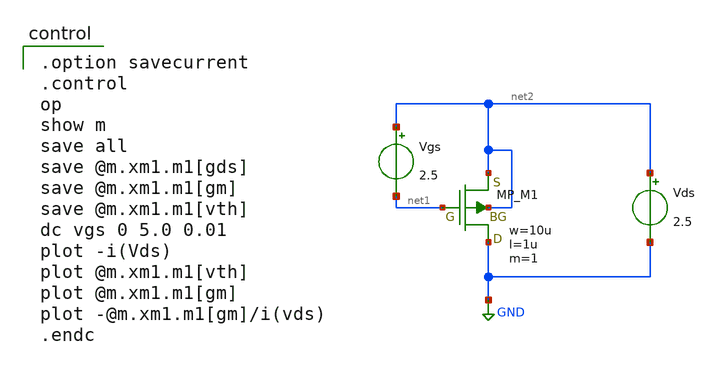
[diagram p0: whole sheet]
** sch_path: OpenSUSI-TR10/opamp/pfet_idvgs.sch
**.subckt pfet_idvgs
Vgs net2 net1 2.5
Vds net2 GND 2.5
XM1 GND net1 net2 net2 PMOS w=10u l=1u as=0 ad=0 ps=0 pd=0 nrd=0 nrs=0 m=1
**** begin user architecture code

.option savecurrent
.control
op
show m
save all
save @m.xm1.m1[gds]
save @m.xm1.m1[gm]
save @m.xm1.m1[vth]
dc vgs 0 5.0 0.01
plot -i(Vds)
plot @m.xm1.m1[vth]
plot @m.xm1.m1[gm]
plot -@m.xm1.m1[gm]/i(vds)
.endc

 .include $::LIB/ip62_models
**** end user architecture code
**.ends
.GLOBAL GND
.end
